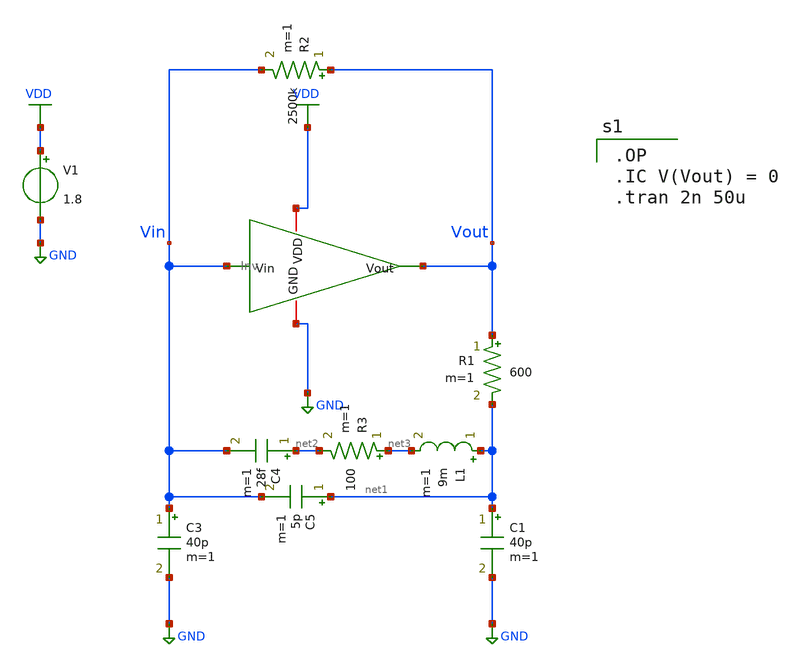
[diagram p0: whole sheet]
** sch_path: pll/xctl_lib_V2/xctl/xschem/Crystal.sch
**.subckt Crystal
R1 Vout net1 600 m=1
R2 Vout Vin 2500k m=1
C1 net1 GND 40p m=1
C3 Vin GND 40p m=1
V1 VDD GND 1.8
L1 net1 net3 9m m=1
R3 net3 net2 100 m=1
C4 net2 Vin 28f m=1
C5 net1 Vin 5p m=1
x1 VDD Vin Vout GND Inv
**** begin user architecture code

** opencircuitdesign pdks install
.lib $::SKYWATER_MODELS/sky130.lib.spice tt



.OP
.IC V(Vout) = 0
.tran 2n 50u

**** end user architecture code
**.ends

* expanding   symbol:  Inv.sym # of pins=4
** sym_path: pll/xctl_lib_V2/xctl/xschem/Inv.sym
** sch_path: pll/xctl_lib_V2/xctl/xschem/Inv.sch
.subckt Inv VDD Vin Vout GND
*.opin Vout
*.ipin Vin
*.iopin VDD
*.iopin GND
XM1 Vout Vin GND GND sky130_fd_pr__nfet_01v8 L=0.15 W=100 nf=1 ad='int((nf+1)/2) * W/nf * 0.29' as='int((nf+2)/2) * W/nf * 0.29'
+ pd='2*int((nf+1)/2) * (W/nf + 0.29)' ps='2*int((nf+2)/2) * (W/nf + 0.29)' nrd='0.29 / W' nrs='0.29 / W'
+ sa=0 sb=0 sd=0 mult=1 m=1
XM2 Vout Vin VDD VDD sky130_fd_pr__nfet_01v8 L=0.15 W=1 nf=1 ad='int((nf+1)/2) * W/nf * 0.29' as='int((nf+2)/2) * W/nf * 0.29'
+ pd='2*int((nf+1)/2) * (W/nf + 0.29)' ps='2*int((nf+2)/2) * (W/nf + 0.29)' nrd='0.29 / W' nrs='0.29 / W'
+ sa=0 sb=0 sd=0 mult=1 m=1
.ends

.GLOBAL GND
.GLOBAL VDD
.end
